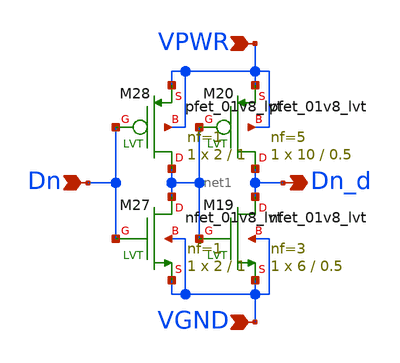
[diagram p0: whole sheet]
** sch_path: xschem/subckts/DAC_driver.sch
**.subckt DAC_driver Dn_d Dn VPWR VGND
*.opin Dn_d
*.ipin Dn
*.ipin VPWR
*.ipin VGND
XM19 Dn_d net1 VGND VGND sky130_fd_pr__nfet_01v8_lvt L=0.5 W=6 nf=3 ad='int((nf+1)/2) * W/nf * 0.29'
+ as='int((nf+2)/2) * W/nf * 0.29' pd='2*int((nf+1)/2) * (W/nf + 0.29)' ps='2*int((nf+2)/2) * (W/nf + 0.29)'
+ nrd='0.29 / W' nrs='0.29 / W' sa=0 sb=0 sd=0 mult=1 m=1
XM20 Dn_d net1 VPWR VPWR sky130_fd_pr__pfet_01v8_lvt L=0.5 W=10 nf=5 ad='int((nf+1)/2) * W/nf * 0.29'
+ as='int((nf+2)/2) * W/nf * 0.29' pd='2*int((nf+1)/2) * (W/nf + 0.29)' ps='2*int((nf+2)/2) * (W/nf + 0.29)'
+ nrd='0.29 / W' nrs='0.29 / W' sa=0 sb=0 sd=0 mult=1 m=1
XM27 net1 Dn VGND VGND sky130_fd_pr__nfet_01v8_lvt L=1 W=2 nf=1 ad='int((nf+1)/2) * W/nf * 0.29' as='int((nf+2)/2) * W/nf * 0.29'
+ pd='2*int((nf+1)/2) * (W/nf + 0.29)' ps='2*int((nf+2)/2) * (W/nf + 0.29)' nrd='0.29 / W' nrs='0.29 / W'
+ sa=0 sb=0 sd=0 mult=1 m=1
XM28 net1 Dn VPWR VPWR sky130_fd_pr__pfet_01v8_lvt L=1 W=2 nf=1 ad='int((nf+1)/2) * W/nf * 0.29' as='int((nf+2)/2) * W/nf * 0.29'
+ pd='2*int((nf+1)/2) * (W/nf + 0.29)' ps='2*int((nf+2)/2) * (W/nf + 0.29)' nrd='0.29 / W' nrs='0.29 / W'
+ sa=0 sb=0 sd=0 mult=1 m=1
**.ends
.end
